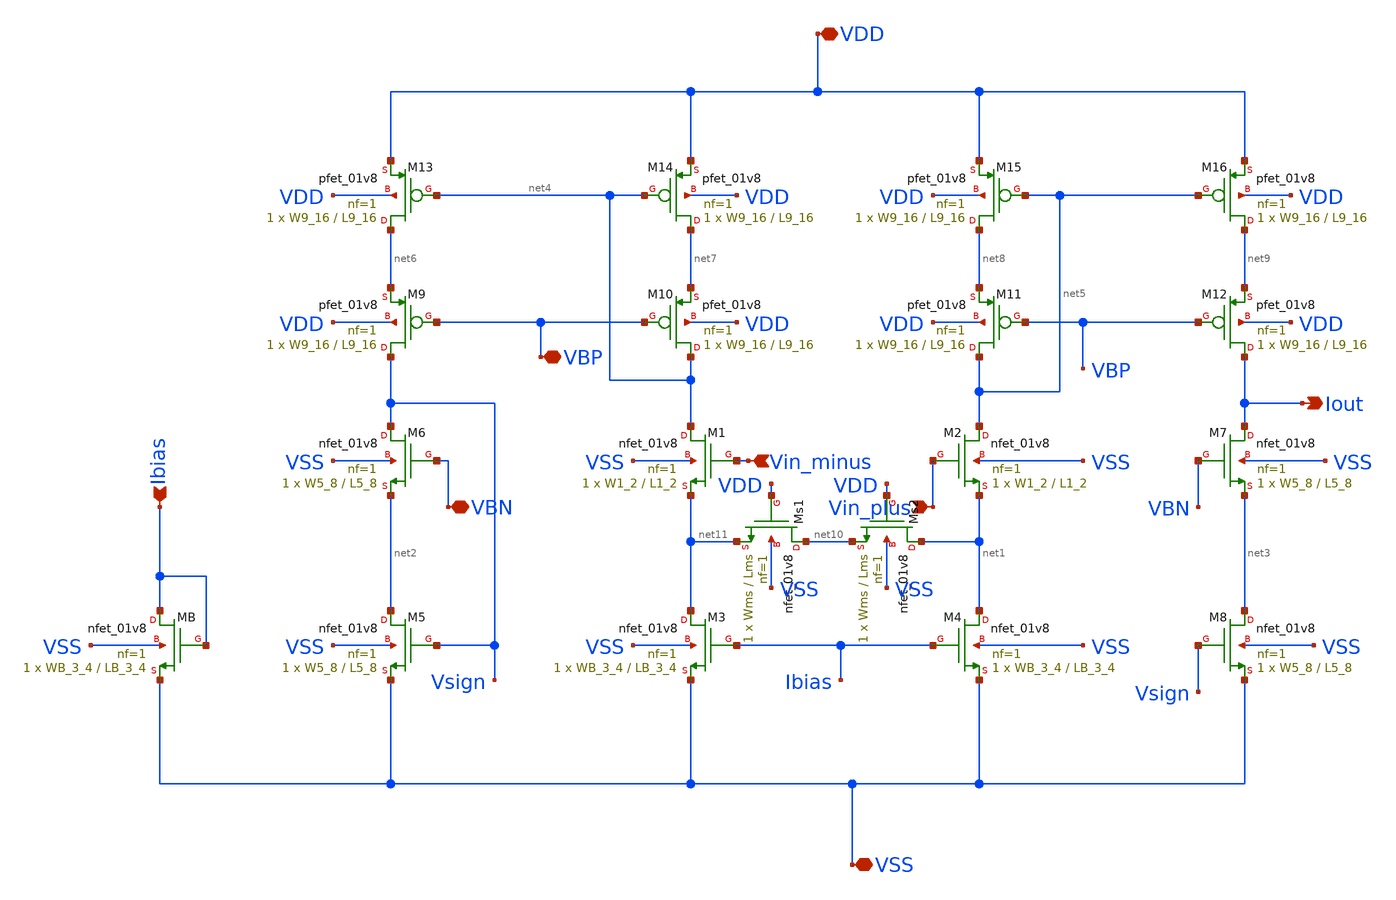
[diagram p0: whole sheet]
** sch_path: OTA/OTA_simb.sch
**.subckt OTA_simb VDD VSS VBN VBP Iout Vin_plus Vin_minus Ibias
*.iopin VDD
*.iopin VSS
*.iopin VBN
*.iopin VBP
*.opin Iout
*.ipin Vin_plus
*.ipin Vin_minus
*.ipin Ibias
XM1 net4 Vin_minus net11 VSS sky130_fd_pr__nfet_01v8 L=L1_2 W=W1_2 nf=1 ad='int((nf+1)/2) * W/nf * 0.29'
+ as='int((nf+2)/2) * W/nf * 0.29' pd='2*int((nf+1)/2) * (W/nf + 0.29)' ps='2*int((nf+2)/2) * (W/nf + 0.29)'
+ nrd='0.29 / W' nrs='0.29 / W' sa=0 sb=0 sd=0 mult=1 m=1
XM2 net5 Vin_plus net1 VSS sky130_fd_pr__nfet_01v8 L=L1_2 W=W1_2 nf=1 ad='int((nf+1)/2) * W/nf * 0.29'
+ as='int((nf+2)/2) * W/nf * 0.29' pd='2*int((nf+1)/2) * (W/nf + 0.29)' ps='2*int((nf+2)/2) * (W/nf + 0.29)'
+ nrd='0.29 / W' nrs='0.29 / W' sa=0 sb=0 sd=0 mult=1 m=1
XM3 net11 Ibias VSS VSS sky130_fd_pr__nfet_01v8 L=LB_3_4 W=WB_3_4 nf=1 ad='int((nf+1)/2) * W/nf * 0.29'
+ as='int((nf+2)/2) * W/nf * 0.29' pd='2*int((nf+1)/2) * (W/nf + 0.29)' ps='2*int((nf+2)/2) * (W/nf + 0.29)'
+ nrd='0.29 / W' nrs='0.29 / W' sa=0 sb=0 sd=0 mult=1 m=1
XM4 net1 Ibias VSS VSS sky130_fd_pr__nfet_01v8 L=LB_3_4 W=WB_3_4 nf=1 ad='int((nf+1)/2) * W/nf * 0.29'
+ as='int((nf+2)/2) * W/nf * 0.29' pd='2*int((nf+1)/2) * (W/nf + 0.29)' ps='2*int((nf+2)/2) * (W/nf + 0.29)'
+ nrd='0.29 / W' nrs='0.29 / W' sa=0 sb=0 sd=0 mult=1 m=1
XM5 net2 Vsign VSS VSS sky130_fd_pr__nfet_01v8 L=L5_8 W=W5_8 nf=1 ad='int((nf+1)/2) * W/nf * 0.29' as='int((nf+2)/2) * W/nf * 0.29'
+ pd='2*int((nf+1)/2) * (W/nf + 0.29)' ps='2*int((nf+2)/2) * (W/nf + 0.29)' nrd='0.29 / W' nrs='0.29 / W'
+ sa=0 sb=0 sd=0 mult=1 m=1
XM6 Vsign VBN net2 VSS sky130_fd_pr__nfet_01v8 L=L5_8 W=W5_8 nf=1 ad='int((nf+1)/2) * W/nf * 0.29' as='int((nf+2)/2) * W/nf * 0.29'
+ pd='2*int((nf+1)/2) * (W/nf + 0.29)' ps='2*int((nf+2)/2) * (W/nf + 0.29)' nrd='0.29 / W' nrs='0.29 / W'
+ sa=0 sb=0 sd=0 mult=1 m=1
XM7 Iout VBN net3 VSS sky130_fd_pr__nfet_01v8 L=L5_8 W=W5_8 nf=1 ad='int((nf+1)/2) * W/nf * 0.29' as='int((nf+2)/2) * W/nf * 0.29'
+ pd='2*int((nf+1)/2) * (W/nf + 0.29)' ps='2*int((nf+2)/2) * (W/nf + 0.29)' nrd='0.29 / W' nrs='0.29 / W'
+ sa=0 sb=0 sd=0 mult=1 m=1
XM8 net3 Vsign VSS VSS sky130_fd_pr__nfet_01v8 L=L5_8 W=W5_8 nf=1 ad='int((nf+1)/2) * W/nf * 0.29' as='int((nf+2)/2) * W/nf * 0.29'
+ pd='2*int((nf+1)/2) * (W/nf + 0.29)' ps='2*int((nf+2)/2) * (W/nf + 0.29)' nrd='0.29 / W' nrs='0.29 / W'
+ sa=0 sb=0 sd=0 mult=1 m=1
XMB Ibias Ibias VSS VSS sky130_fd_pr__nfet_01v8 L=LB_3_4 W=WB_3_4 nf=1 ad='int((nf+1)/2) * W/nf * 0.29'
+ as='int((nf+2)/2) * W/nf * 0.29' pd='2*int((nf+1)/2) * (W/nf + 0.29)' ps='2*int((nf+2)/2) * (W/nf + 0.29)'
+ nrd='0.29 / W' nrs='0.29 / W' sa=0 sb=0 sd=0 mult=1 m=1
XM9 Vsign VBP net6 VDD sky130_fd_pr__pfet_01v8 L=L9_16 W=W9_16 nf=1 ad='int((nf+1)/2) * W/nf * 0.29'
+ as='int((nf+2)/2) * W/nf * 0.29' pd='2*int((nf+1)/2) * (W/nf + 0.29)' ps='2*int((nf+2)/2) * (W/nf + 0.29)'
+ nrd='0.29 / W' nrs='0.29 / W' sa=0 sb=0 sd=0 mult=1 m=1
XM10 net4 VBP net7 VDD sky130_fd_pr__pfet_01v8 L=L9_16 W=W9_16 nf=1 ad='int((nf+1)/2) * W/nf * 0.29'
+ as='int((nf+2)/2) * W/nf * 0.29' pd='2*int((nf+1)/2) * (W/nf + 0.29)' ps='2*int((nf+2)/2) * (W/nf + 0.29)'
+ nrd='0.29 / W' nrs='0.29 / W' sa=0 sb=0 sd=0 mult=1 m=1
XM11 net5 VBP net8 VDD sky130_fd_pr__pfet_01v8 L=L9_16 W=W9_16 nf=1 ad='int((nf+1)/2) * W/nf * 0.29'
+ as='int((nf+2)/2) * W/nf * 0.29' pd='2*int((nf+1)/2) * (W/nf + 0.29)' ps='2*int((nf+2)/2) * (W/nf + 0.29)'
+ nrd='0.29 / W' nrs='0.29 / W' sa=0 sb=0 sd=0 mult=1 m=1
XM12 Iout VBP net9 VDD sky130_fd_pr__pfet_01v8 L=L9_16 W=W9_16 nf=1 ad='int((nf+1)/2) * W/nf * 0.29'
+ as='int((nf+2)/2) * W/nf * 0.29' pd='2*int((nf+1)/2) * (W/nf + 0.29)' ps='2*int((nf+2)/2) * (W/nf + 0.29)'
+ nrd='0.29 / W' nrs='0.29 / W' sa=0 sb=0 sd=0 mult=1 m=1
XM13 net6 net4 VDD VDD sky130_fd_pr__pfet_01v8 L=L9_16 W=W9_16 nf=1 ad='int((nf+1)/2) * W/nf * 0.29'
+ as='int((nf+2)/2) * W/nf * 0.29' pd='2*int((nf+1)/2) * (W/nf + 0.29)' ps='2*int((nf+2)/2) * (W/nf + 0.29)'
+ nrd='0.29 / W' nrs='0.29 / W' sa=0 sb=0 sd=0 mult=1 m=1
XM14 net7 net4 VDD VDD sky130_fd_pr__pfet_01v8 L=L9_16 W=W9_16 nf=1 ad='int((nf+1)/2) * W/nf * 0.29'
+ as='int((nf+2)/2) * W/nf * 0.29' pd='2*int((nf+1)/2) * (W/nf + 0.29)' ps='2*int((nf+2)/2) * (W/nf + 0.29)'
+ nrd='0.29 / W' nrs='0.29 / W' sa=0 sb=0 sd=0 mult=1 m=1
XM15 net8 net5 VDD VDD sky130_fd_pr__pfet_01v8 L=L9_16 W=W9_16 nf=1 ad='int((nf+1)/2) * W/nf * 0.29'
+ as='int((nf+2)/2) * W/nf * 0.29' pd='2*int((nf+1)/2) * (W/nf + 0.29)' ps='2*int((nf+2)/2) * (W/nf + 0.29)'
+ nrd='0.29 / W' nrs='0.29 / W' sa=0 sb=0 sd=0 mult=1 m=1
XM16 net9 net5 VDD VDD sky130_fd_pr__pfet_01v8 L=L9_16 W=W9_16 nf=1 ad='int((nf+1)/2) * W/nf * 0.29'
+ as='int((nf+2)/2) * W/nf * 0.29' pd='2*int((nf+1)/2) * (W/nf + 0.29)' ps='2*int((nf+2)/2) * (W/nf + 0.29)'
+ nrd='0.29 / W' nrs='0.29 / W' sa=0 sb=0 sd=0 mult=1 m=1
XMs1 net10 VDD net11 VSS sky130_fd_pr__nfet_01v8 L=Lms W=Wms nf=1 ad='int((nf+1)/2) * W/nf * 0.29' as='int((nf+2)/2) * W/nf * 0.29'
+ pd='2*int((nf+1)/2) * (W/nf + 0.29)' ps='2*int((nf+2)/2) * (W/nf + 0.29)' nrd='0.29 / W' nrs='0.29 / W'
+ sa=0 sb=0 sd=0 mult=1 m=1
XMs2 net1 VDD net10 VSS sky130_fd_pr__nfet_01v8 L=Lms W=Wms nf=1 ad='int((nf+1)/2) * W/nf * 0.29' as='int((nf+2)/2) * W/nf * 0.29'
+ pd='2*int((nf+1)/2) * (W/nf + 0.29)' ps='2*int((nf+2)/2) * (W/nf + 0.29)' nrd='0.29 / W' nrs='0.29 / W'
+ sa=0 sb=0 sd=0 mult=1 m=1
**.ends
.end
